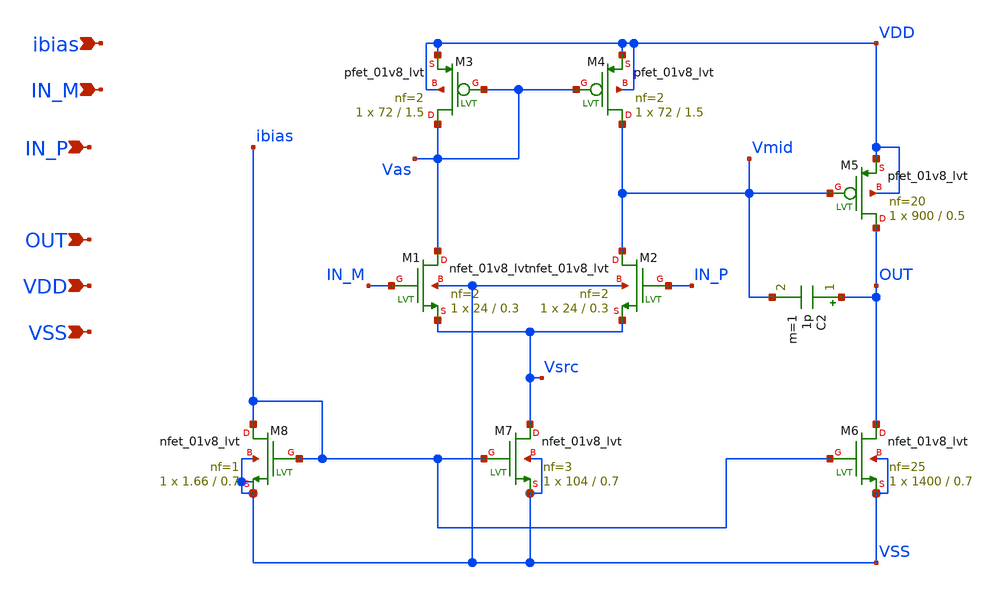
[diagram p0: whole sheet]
** sch_path: OTA_erroramp_am.sch
**.subckt OTA_erroramp_am IN_M IN_P OUT VDD VSS ibias
*.ipin IN_M
*.ipin IN_P
*.ipin OUT
*.ipin VDD
*.ipin VSS
*.ipin ibias
XM1 Vas IN_M Vsrc VSS sky130_fd_pr__nfet_01v8_lvt L=0.3 W=24 nf=2 ad='int((nf+1)/2) * W/nf * 0.29' as='int((nf+2)/2) * W/nf * 0.29'
+ pd='2*int((nf+1)/2) * (W/nf + 0.29)' ps='2*int((nf+2)/2) * (W/nf + 0.29)' nrd='0.29 / W' nrs='0.29 / W'
+ sa=0 sb=0 sd=0 mult=1 m=1
XM2 Vmid IN_P Vsrc VSS sky130_fd_pr__nfet_01v8_lvt L=0.3 W=24 nf=2 ad='int((nf+1)/2) * W/nf * 0.29' as='int((nf+2)/2) * W/nf * 0.29'
+ pd='2*int((nf+1)/2) * (W/nf + 0.29)' ps='2*int((nf+2)/2) * (W/nf + 0.29)' nrd='0.29 / W' nrs='0.29 / W'
+ sa=0 sb=0 sd=0 mult=1 m=1
XM3 Vas Vas VDD VDD sky130_fd_pr__pfet_01v8_lvt L=1.5 W=72 nf=2 ad='int((nf+1)/2) * W/nf * 0.29' as='int((nf+2)/2) * W/nf * 0.29'
+ pd='2*int((nf+1)/2) * (W/nf + 0.29)' ps='2*int((nf+2)/2) * (W/nf + 0.29)' nrd='0.29 / W' nrs='0.29 / W'
+ sa=0 sb=0 sd=0 mult=1 m=1
XM4 Vmid Vas VDD VDD sky130_fd_pr__pfet_01v8_lvt L=1.5 W=72 nf=2 ad='int((nf+1)/2) * W/nf * 0.29' as='int((nf+2)/2) * W/nf * 0.29'
+ pd='2*int((nf+1)/2) * (W/nf + 0.29)' ps='2*int((nf+2)/2) * (W/nf + 0.29)' nrd='0.29 / W' nrs='0.29 / W'
+ sa=0 sb=0 sd=0 mult=1 m=1
XM5 OUT Vmid VDD VDD sky130_fd_pr__pfet_01v8_lvt L=0.5 W=900 nf=20 ad='int((nf+1)/2) * W/nf * 0.29' as='int((nf+2)/2) * W/nf * 0.29'
+ pd='2*int((nf+1)/2) * (W/nf + 0.29)' ps='2*int((nf+2)/2) * (W/nf + 0.29)' nrd='0.29 / W' nrs='0.29 / W'
+ sa=0 sb=0 sd=0 mult=1 m=1
XM6 OUT ibias VSS VSS sky130_fd_pr__nfet_01v8_lvt L=0.7 W=1400 nf=25 ad='int((nf+1)/2) * W/nf * 0.29'
+ as='int((nf+2)/2) * W/nf * 0.29' pd='2*int((nf+1)/2) * (W/nf + 0.29)' ps='2*int((nf+2)/2) * (W/nf + 0.29)'
+ nrd='0.29 / W' nrs='0.29 / W' sa=0 sb=0 sd=0 mult=1 m=1
XM7 Vsrc ibias VSS VSS sky130_fd_pr__nfet_01v8_lvt L=0.7 W=104 nf=3 ad='int((nf+1)/2) * W/nf * 0.29'
+ as='int((nf+2)/2) * W/nf * 0.29' pd='2*int((nf+1)/2) * (W/nf + 0.29)' ps='2*int((nf+2)/2) * (W/nf + 0.29)'
+ nrd='0.29 / W' nrs='0.29 / W' sa=0 sb=0 sd=0 mult=1 m=1
XM8 ibias ibias VSS VSS sky130_fd_pr__nfet_01v8_lvt L=0.7 W=1.66 nf=1 ad='int((nf+1)/2) * W/nf * 0.29'
+ as='int((nf+2)/2) * W/nf * 0.29' pd='2*int((nf+1)/2) * (W/nf + 0.29)' ps='2*int((nf+2)/2) * (W/nf + 0.29)'
+ nrd='0.29 / W' nrs='0.29 / W' sa=0 sb=0 sd=0 mult=1 m=1
C2 OUT Vmid 1p m=1
**.ends
.end
